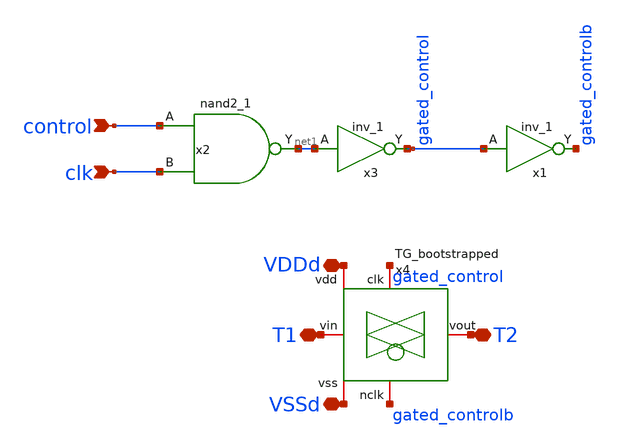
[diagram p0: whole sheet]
** sch_path: designs/libs/core_TGB_swmatrix/TGB_swmatrix.sch
**.subckt TGB_swmatrix T1 T2 VDDd control clk VSSd
*.iopin T1
*.iopin T2
*.iopin VDDd
*.ipin control
*.ipin clk
*.iopin VSSd
x1 gated_control VSSd VDDd VSSd VDDd gated_controlb gf180mcu_fd_sc_mcu9t5v0__inv_1
x2 control clk VSSd VDDd VSSd VDDd net1 gf180mcu_fd_sc_mcu9t5v0__nand2_1
x3 net1 VSSd VDDd VSSd VDDd gated_control gf180mcu_fd_sc_mcu9t5v0__inv_1
x4 VDDd VSSd gated_control gated_controlb T1 T2 TG_bootstrapped
**.ends
.end
